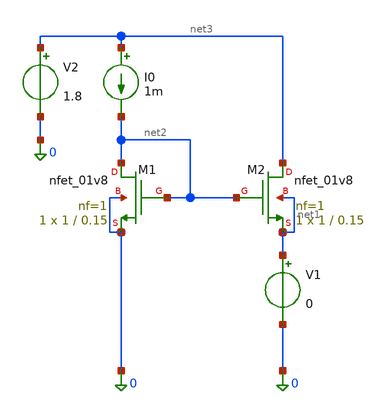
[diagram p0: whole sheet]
** sch_path: src/analog_mac/untitled.sch
**.subckt untitled
XM1 net2 net2 0 0 sky130_fd_pr__nfet_01v8 L=0.15 W=1 nf=1 ad='int((1 + 1)/2) * 1 / 1 * 0.29' as='int((1 + 2)/2) * 1 / 1 * 0.29'
+ pd='2*int((1 + 1)/2) * (1 / 1 + 0.29)' ps='2*int((1 + 2)/2) * (1 / 1 + 0.29)' nrd='0.29 / 1 ' nrs='0.29 / 1 '
+ sa=0 sb=0 sd=0 mult=1 m=1
XM2 net3 net2 net1 net1 sky130_fd_pr__nfet_01v8 L=0.15 W=1 nf=1 ad='int((1 + 1)/2) * 1 / 1 * 0.29' as='int((1 + 2)/2) * 1 / 1 * 0.29'
+ pd='2*int((1 + 1)/2) * (1 / 1 + 0.29)' ps='2*int((1 + 2)/2) * (1 / 1 + 0.29)' nrd='0.29 / 1 ' nrs='0.29 / 1 '
+ sa=0 sb=0 sd=0 mult=1 m=1
V1 net1 0 0
V2 net3 0 1.8
I0 net3 net2 1m
**.ends
.end
